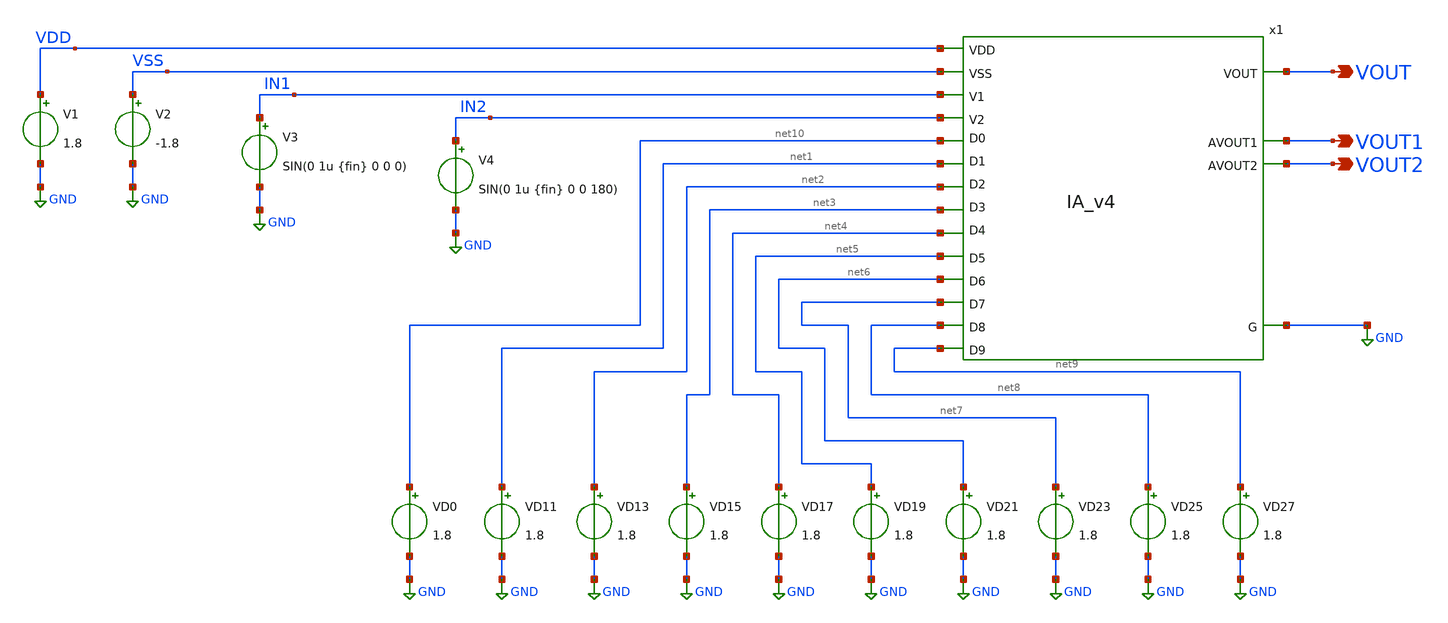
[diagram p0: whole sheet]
** sch_path: xschem/IA_v4_testbench.sch
**.subckt IA_v4_testbench VOUT VOUT1 VOUT2
*.opin VOUT
*.opin VOUT1
*.opin VOUT2
V1 VDD GND 1.8
V2 VSS GND -1.8
V3 IN1 GND SIN(0 1u {fin} 0 0 0)
V4 IN2 GND SIN(0 1u {fin} 0 0 180)
VD0 net10 GND 1.8
VD11 net1 GND 1.8
VD13 net2 GND 1.8
VD15 net3 GND 1.8
VD17 net4 GND 1.8
VD19 net5 GND 1.8
VD21 net6 GND 1.8
VD23 net7 GND 1.8
VD25 net8 GND 1.8
VD27 net9 GND 1.8
x1 VDD VSS GND IN1 IN2 net10 net1 net2 net3 net4 net5 net6 net7 net8 net9 VOUT1 VOUT2 VOUT IA_v4
**** begin user architecture code

.include /foss/designs/sky130_hcmus_ip__instramp/xschem/layout/IA_v4.pex.spice
.param fin = 10K
.control
save all
tran 0.1u 100u
meas tran minv MIN v(vout)
meas tran maxv MAX v(vout)
let gain = ((abs(maxv)+abs(minv))/(2e-6))
print gain
write IA_v4_testbench.raw
.endc

.lib $::SKYWATER_MODELS/sky130.lib.spice tt
**** end user architecture code
**.ends
.GLOBAL GND
.end
